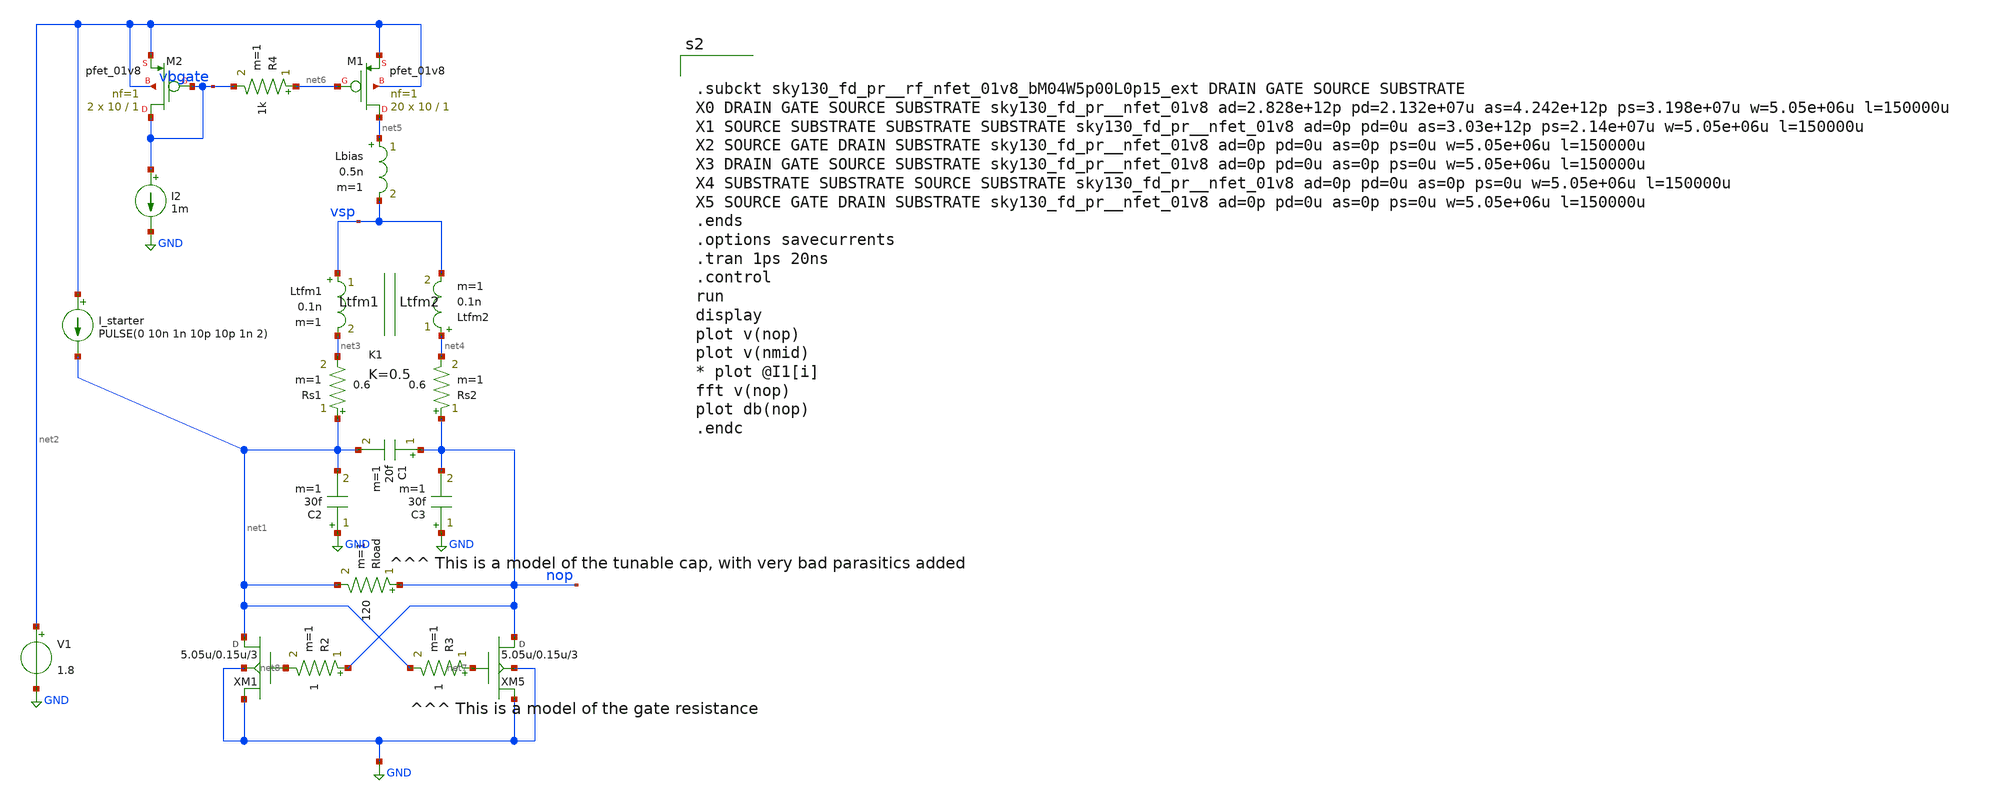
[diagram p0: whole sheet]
** sch_path: xschem/OSC_HF1.sch
**.subckt OSC_HF1
XM5 nop net7 GND GND sky130_fd_pr__rf_nfet_01v8_bM04W5p00L0p15_ext w=5.05u l=0.15u m=3
XM1 net1 net8 GND GND sky130_fd_pr__rf_nfet_01v8_bM04W5p00L0p15_ext w=5.05u l=0.15u m=3
Ltfm1 vsp net3 0.1n m=1
Ltfm2 net4 vsp 0.1n m=1
V1 net2 GND 1.8
I_starter net2 net1 PULSE(0 10n 1n 10p 10p 1n 2)
R2 nop net8 1 m=1
R3 net7 net1 1 m=1
Rs1 net1 net3 0.6 m=1
K1 Ltfm1 Ltfm2 0.5
Rload nop net1 120 m=1
Rs2 nop net4 0.6 m=1
C1 nop net1 20f m=1
C2 GND net1 30f m=1
C3 GND nop 30f m=1
XM1 net5 net6 net2 net2 sky130_fd_pr__pfet_01v8 L=1 W=10 nf=1 ad='int((nf+1)/2) * W/nf * 0.29' as='int((nf+2)/2) * W/nf * 0.29'
+ pd='2*int((nf+1)/2) * (W/nf + 0.29)' ps='2*int((nf+2)/2) * (W/nf + 0.29)' nrd='0.29 / W' nrs='0.29 / W'
+ sa=0 sb=0 sd=0 mult=20 m=20
XM2 vbgate vbgate net2 net2 sky130_fd_pr__pfet_01v8 L=1 W=10 nf=1 ad='int((nf+1)/2) * W/nf * 0.29' as='int((nf+2)/2) * W/nf * 0.29'
+ pd='2*int((nf+1)/2) * (W/nf + 0.29)' ps='2*int((nf+2)/2) * (W/nf + 0.29)' nrd='0.29 / W' nrs='0.29 / W'
+ sa=0 sb=0 sd=0 mult=2 m=2
I2 vbgate GND 1m
Lbias net5 vsp 0.5n m=1
R4 net6 vbgate 1k m=1
**** begin user architecture code
.lib $::SKYWATER_MODELS/sky130.lib.spice ss
* .include $::PDKPATH/libs.ref/sky130_fd_sc_hvl/spice/sky130_fd_sc_hvl.spice



.subckt sky130_fd_pr__rf_nfet_01v8_bM04W5p00L0p15_ext DRAIN GATE SOURCE SUBSTRATE
X0 DRAIN GATE SOURCE SUBSTRATE sky130_fd_pr__nfet_01v8 ad=2.828e+12p pd=2.132e+07u as=4.242e+12p
+ ps=3.198e+07u w=5.05e+06u l=150000u
X1 SOURCE SUBSTRATE SUBSTRATE SUBSTRATE sky130_fd_pr__nfet_01v8 ad=0p pd=0u as=3.03e+12p
+ ps=2.14e+07u w=5.05e+06u l=150000u
X2 SOURCE GATE DRAIN SUBSTRATE sky130_fd_pr__nfet_01v8 ad=0p pd=0u as=0p ps=0u w=5.05e+06u l=150000u
X3 DRAIN GATE SOURCE SUBSTRATE sky130_fd_pr__nfet_01v8 ad=0p pd=0u as=0p ps=0u w=5.05e+06u l=150000u
X4 SUBSTRATE SUBSTRATE SOURCE SUBSTRATE sky130_fd_pr__nfet_01v8 ad=0p pd=0u as=0p ps=0u w=5.05e+06u
+ l=150000u
X5 SOURCE GATE DRAIN SUBSTRATE sky130_fd_pr__nfet_01v8 ad=0p pd=0u as=0p ps=0u w=5.05e+06u l=150000u
.ends
.options savecurrents
.tran 1ps 20ns
.control
run
display
plot v(nop)
plot v(nmid)
* plot @I1[i]
fft v(nop)
plot db(nop)
.endc


**** end user architecture code
**.ends
.GLOBAL GND
.end
